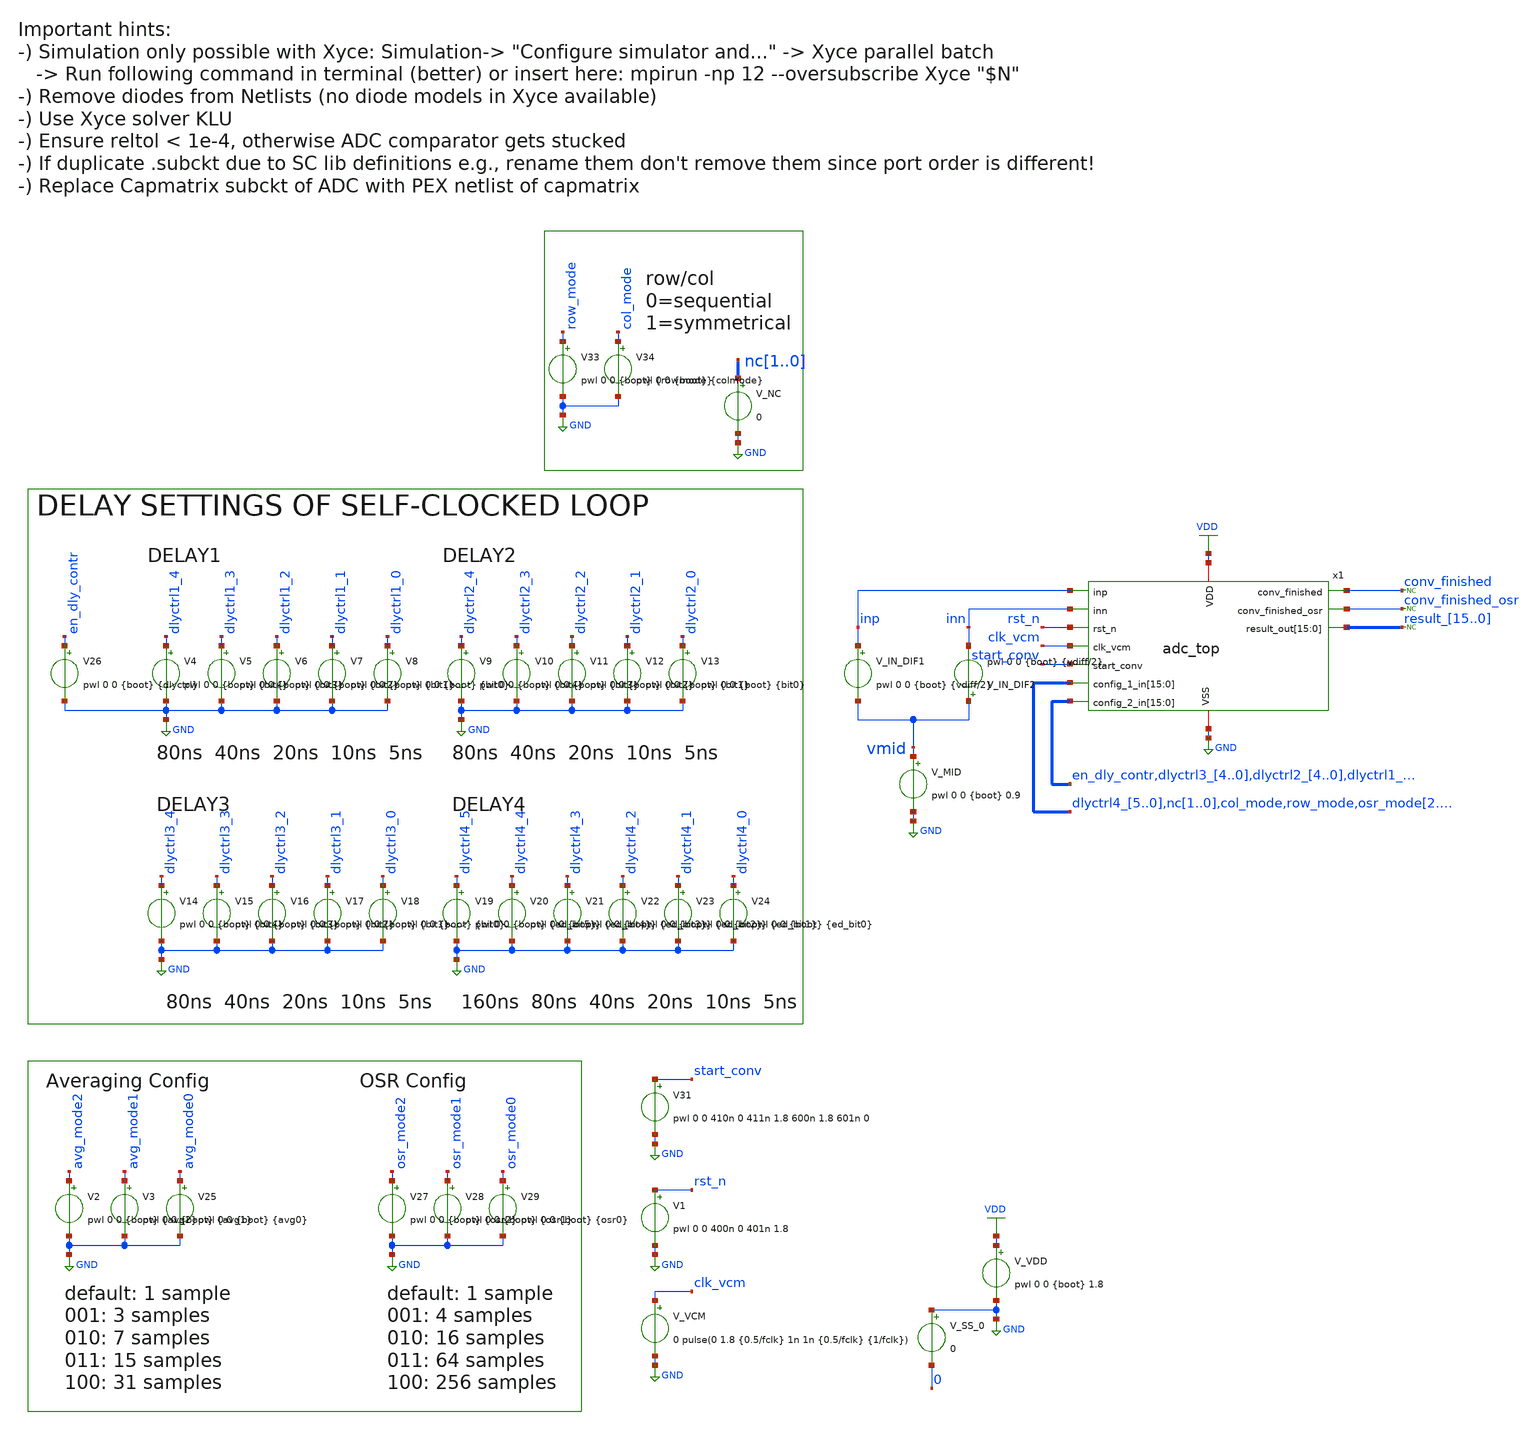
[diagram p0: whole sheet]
** sch_path: xschem/adc_top_tb.sch
**.subckt adc_top_tb
V_VDD VDD GND pwl 0 0 {boot} 1.8
V_MID vmid GND pwl 0 0 {boot} 0.9
* noconn result_[15..0]
* noconn conv_finished
V_IN_DIF1 inp vmid pwl 0 0 {boot} {vdiff/2}
V_IN_DIF2 vmid inn pwl 0 0 {boot} {vdiff/2}
* noconn conv_finished_osr
V_VCM clk_vcm GND 0 pulse(0 1.8 {0.5/fclk} 1n 1n {0.5/fclk} {1/fclk})
V1 rst_n GND pwl 0 0 400n 0 401n 1.8
V31 start_conv GND pwl 0 0 410n 0 411n 1.8 600n 1.8 601n 0
V33 row_mode GND pwl 0 0 {boot} {rowmode}
V34 col_mode GND pwl 0 0 {boot} {colmode}
x1 VDD GND inp inn rst_n clk_vcm start_conv conv_finished conv_finished_osr dlyctrl4_5 dlyctrl4_4
+ dlyctrl4_3 dlyctrl4_2 dlyctrl4_1 dlyctrl4_0 nc1 nc0 col_mode row_mode osr_mode2 osr_mode1 osr_mode0 avg_mode2
+ avg_mode1 avg_mode0 en_dly_contr dlyctrl3_4 dlyctrl3_3 dlyctrl3_2 dlyctrl3_1 dlyctrl3_0 dlyctrl2_4 dlyctrl2_3
+ dlyctrl2_2 dlyctrl2_1 dlyctrl2_0 dlyctrl1_4 dlyctrl1_3 dlyctrl1_2 dlyctrl1_1 dlyctrl1_0 result_15 result_14
+ result_13 result_12 result_11 result_10 result_9 result_8 result_7 result_6 result_5 result_4 result_3
+ result_2 result_1 result_0 adc_top
V_NC nc1 GND 0
V_SS_0 GND 0 0
V2 avg_mode2 GND pwl 0 0 {boot} {avg2}
V3 avg_mode1 GND pwl 0 0 {boot} {avg1}
V25 avg_mode0 GND pwl 0 0 {boot} {avg0}
V27 osr_mode2 GND pwl 0 0 {boot} {osr2}
V28 osr_mode1 GND pwl 0 0 {boot} {osr1}
V29 osr_mode0 GND pwl 0 0 {boot} {osr0}
V4 dlyctrl1_4 GND pwl 0 0 {boot} {bit4}
V5 dlyctrl1_3 GND pwl 0 0 {boot} {bit3}
V6 dlyctrl1_2 GND pwl 0 0 {boot} {bit2}
V7 dlyctrl1_1 GND pwl 0 0 {boot} {bit1}
V8 dlyctrl1_0 GND pwl 0 0 {boot} {bit0}
V26 en_dly_contr GND pwl 0 0 {boot} {dlyctrl}
V9 dlyctrl2_4 GND pwl 0 0 {boot} {bit4}
V10 dlyctrl2_3 GND pwl 0 0 {boot} {bit3}
V11 dlyctrl2_2 GND pwl 0 0 {boot} {bit2}
V12 dlyctrl2_1 GND pwl 0 0 {boot} {bit1}
V13 dlyctrl2_0 GND pwl 0 0 {boot} {bit0}
V19 dlyctrl4_5 GND pwl 0 0 {boot} {ed_bit5}
V20 dlyctrl4_4 GND pwl 0 0 {boot} {ed_bit4}
V21 dlyctrl4_3 GND pwl 0 0 {boot} {ed_bit3}
V22 dlyctrl4_2 GND pwl 0 0 {boot} {ed_bit2}
V23 dlyctrl4_1 GND pwl 0 0 {boot} {ed_bit1}
V24 dlyctrl4_0 GND pwl 0 0 {boot} {ed_bit0}
V14 dlyctrl3_4 GND pwl 0 0 {boot} {bit4}
V15 dlyctrl3_3 GND pwl 0 0 {boot} {bit3}
V16 dlyctrl3_2 GND pwl 0 0 {boot} {bit2}
V17 dlyctrl3_1 GND pwl 0 0 {boot} {bit1}
V18 dlyctrl3_0 GND pwl 0 0 {boot} {bit0}
**** begin user architecture code

** opencircuitdesign pdks install
.lib $::SKYWATER_MODELS/sky130.lib.spice tt








* ngspice commands
.include /foss/designs/sky130_adc_202311/xschem/adc_top_sim.spice

****************
* Misc
****************
.param fclk=32768
.param vdiff=200m
.param boot=1u

****************
* Delay Config
****************
.param dlyctrl = 1.8

* delay 1-3
.param bit0 = 0
.param bit1 = 1.8
.param bit2 = 0
.param bit3 = 0
.param bit4 = 0

* edgedetect pulse
.param ed_bit0 = 0
.param ed_bit1 = 0
.param ed_bit2 = 1.8
.param ed_bit3 = 1.8
.param ed_bit4 = 0
.param ed_bit5 = 0

****************
* Averaging Config
****************
.param avg0 = 0
.param avg1 = 0
.param avg2 = 0

****************
* OSR Config
****************
.param osr0 = 0
.param osr1 = 0
.param osr2 = 0


****************
* Row Column
* sequential or symmetric
****************
.param rowmode = 0
.param colmode = 0

.save all
.control
.option abstol=1.0e-10
.option gmin=1.0e-9
.option reltol=0.01
.option vntol=1.0e-4
.option rshunt=1.0e9

set num_threads=11
tran 10n 2u
plot inp inn rst_n start_conv conv_finished
plot start_conv x1.clk_dig x1.clk_comp
plot x1.pctop x1.nctop x1.comparator_result
plot x1.pctop-x1.nctop

let k = length(time) - 1

* Print the result vector at the end of tran
print result15[k] result14[k] result13[k] result12[k] result11[k] result10[k] result9[k] result8[k]
+ result7[k] result6[k] result5[k] result4[k] result3[k] result2[k] result1[k] result0[k]
* Print the result diff-voltage at the end of tran
print
+ ((result15[k]*2048+result14[k]*1024+result13[k]*512+result12[k]*256+result11[k]*128+result10[k]*64+result9[k]*32+result8[k]*16+result7[k]*8+result6[k]*4+result5[k]*2+result4[k]*1+result3[k]*0.5+result2[k]*0.25+result1[k]*0.125+result0[k]*0.0625)-2048*1.8)/2048

write adc_top_tb.raw

.endc



**** end user architecture code
**.ends
.GLOBAL VDD
.GLOBAL GND
.end
